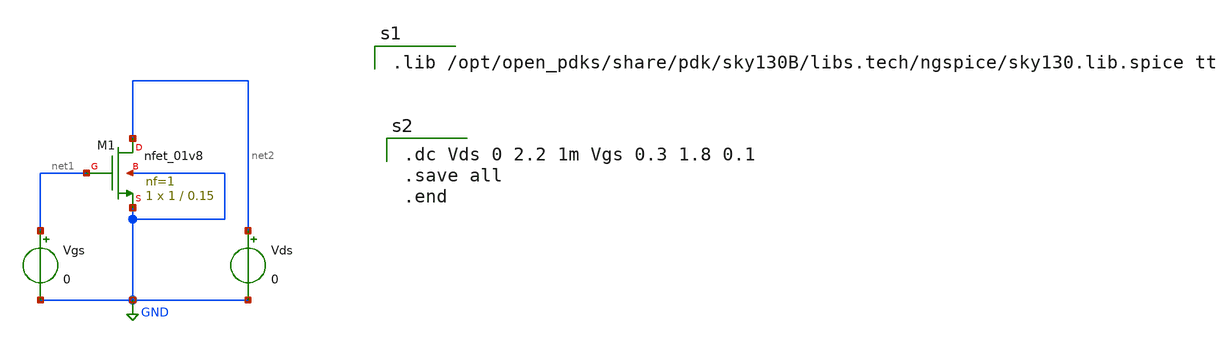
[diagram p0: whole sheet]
** sch_path: projects/transistor/transistor.sch
**.subckt transistor
XM1 net2 net1 GND GND sky130_fd_pr__nfet_01v8 L=0.15 W=1 nf=1 ad='int((nf+1)/2) * W/nf * 0.29' as='int((nf+2)/2) * W/nf * 0.29'
+ pd='2*int((nf+1)/2) * (W/nf + 0.29)' ps='2*int((nf+2)/2) * (W/nf + 0.29)' nrd='0.29 / W' nrs='0.29 / W'
+ sa=0 sb=0 sd=0 mult=1 m=1
Vgs net1 GND 0
Vds net2 GND 0
**** begin user architecture code

.lib /opt/open_pdks/share/pdk/sky130B/libs.tech/ngspice/sky130.lib.spice tt


.dc Vds 0 2.2 1m Vgs 0.3 1.8 0.1
.save all
.end

**** end user architecture code
**.ends
.GLOBAL GND
.end
